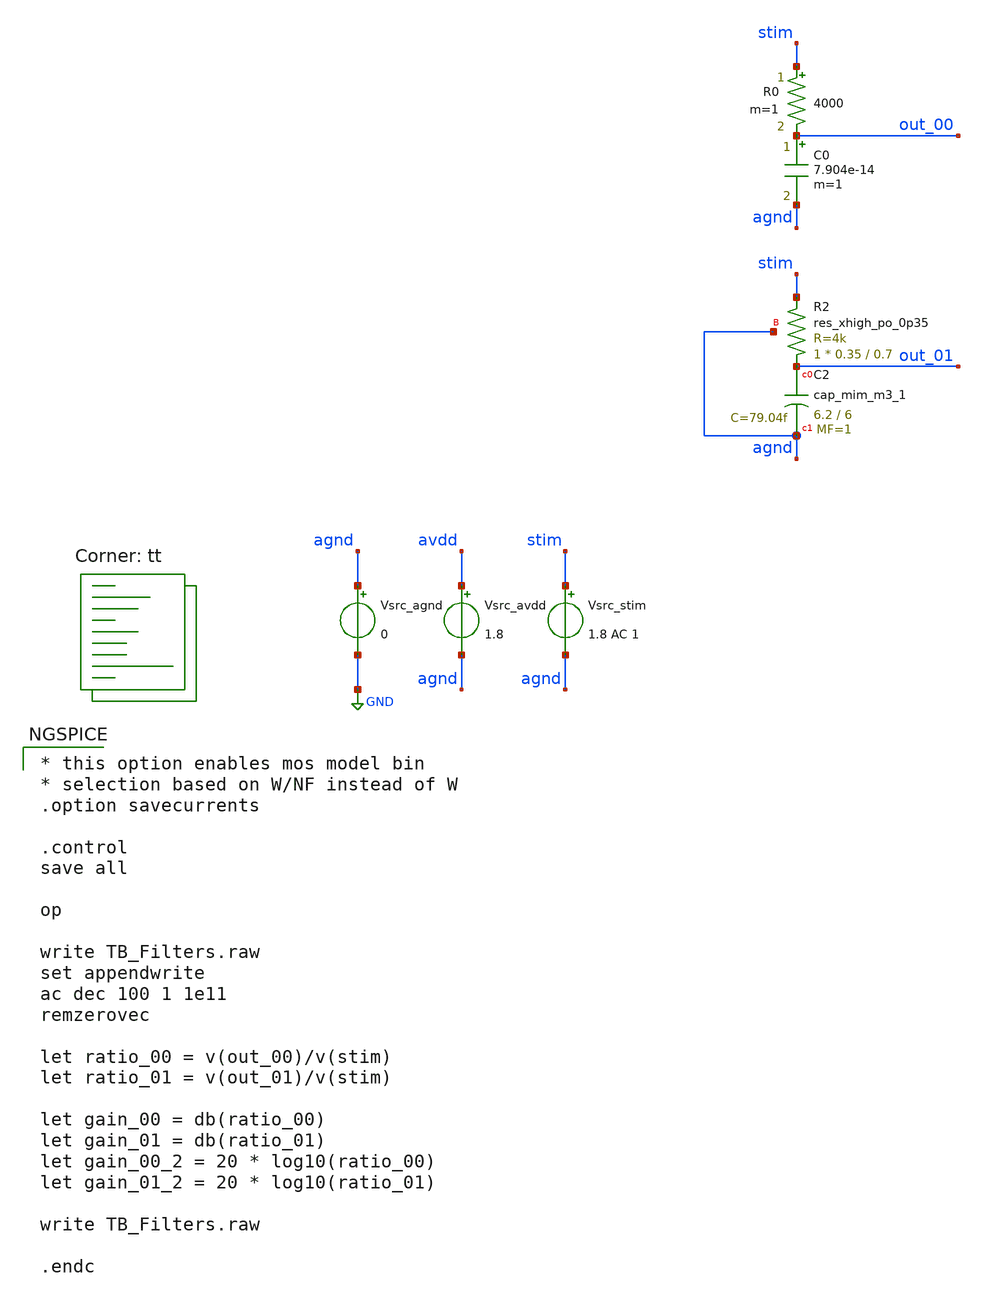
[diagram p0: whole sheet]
** sch_path: LPF/TB_Filters.sch
**.subckt TB_Filters
Vsrc_agnd agnd GND 0
Vsrc_avdd avdd agnd 1.8
Vsrc_stim stim agnd 1.8 AC 1
XC2 out_01 agnd sky130_fd_pr__cap_mim_m3_1 W=6.2 L=6 MF=1 m=1
XR2 out_01 stim agnd sky130_fd_pr__res_xhigh_po_0p35 L=0.7 mult=1 m=1
R0 stim out_00 4000 m=1
C0 out_00 agnd 7.904e-14 m=1
**** begin user architecture code
.lib $::SKYWATER_MODELS/sky130.lib.spice tt

* this option enables mos model bin
* selection based on W/NF instead of W
.option savecurrents

.control
save all

op

write TB_Filters.raw
set appendwrite
ac dec 100 1 1e11
remzerovec

let ratio_00 = v(out_00)/v(stim)
let ratio_01 = v(out_01)/v(stim)

let gain_00 = db(ratio_00)
let gain_01 = db(ratio_01)
let gain_00_2 = 20 * log10(ratio_00)
let gain_01_2 = 20 * log10(ratio_01)

write TB_Filters.raw

.endc


**** end user architecture code
**.ends
.GLOBAL GND
.end
